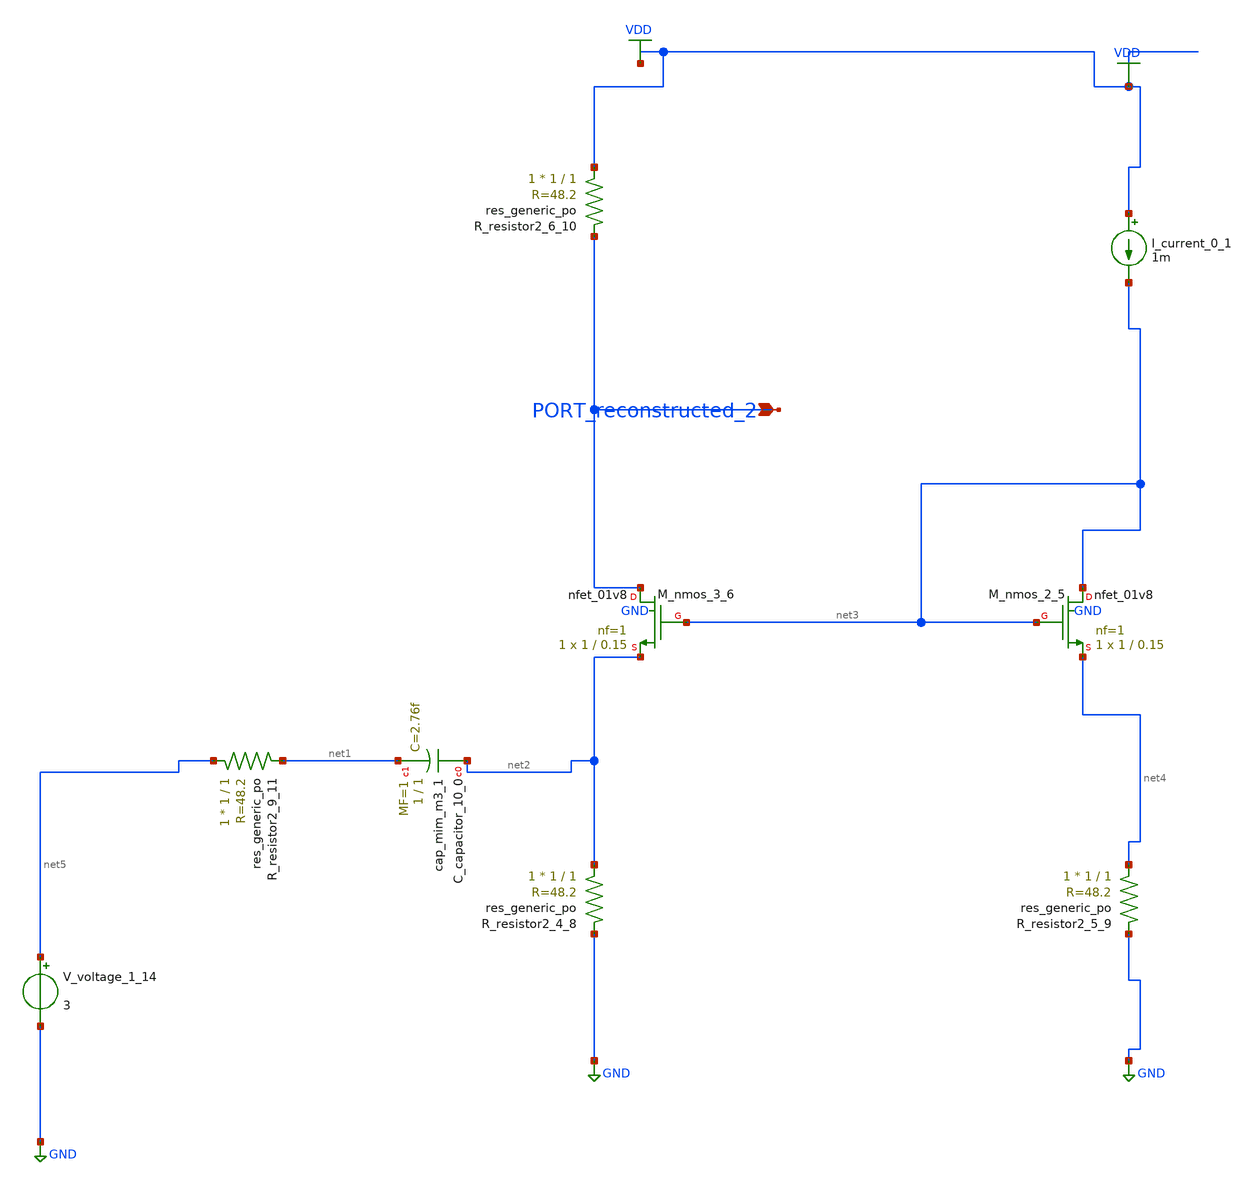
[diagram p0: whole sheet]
** sch_path: schematics/AMSNet/312.sch
**.subckt 312 PORT_reconstructed_2
*.ipin PORT_reconstructed_2
XC_capacitor_10_0 net2 net1 sky130_fd_pr__cap_mim_m3_1 W=1 L=1 MF=1 m=1
I_current_0_1 VDD net3 1m
XM_nmos_2_5 net3 net3 net4 GND sky130_fd_pr__nfet_01v8 L=0.15 W=1 nf=1 ad='int((1 + 1)/2) * 1 / 1 * 0.29'
+ as='int((1 + 2)/2) * 1 / 1 * 0.29' pd='2*int((1 + 1)/2) * (1 / 1 + 0.29)' ps='2*int((1 + 2)/2) * (1 / 1 + 0.29)'
+ nrd='0.29 / 1 ' nrs='0.29 / 1 ' sa=0 sb=0 sd=0 mult=1 m=1
XM_nmos_3_6 PORT_reconstructed_2 net3 net2 GND sky130_fd_pr__nfet_01v8 L=0.15 W=1 nf=1 ad='int((1 + 1)/2) * 1 / 1 * 0.29'
+ as='int((1 + 2)/2) * 1 / 1 * 0.29' pd='2*int((1 + 1)/2) * (1 / 1 + 0.29)' ps='2*int((1 + 2)/2) * (1 / 1 + 0.29)'
+ nrd='0.29 / 1 ' nrs='0.29 / 1 ' sa=0 sb=0 sd=0 mult=1 m=1
XR_resistor2_4_8 net2 GND sky130_fd_pr__res_generic_po W=1 L=1 m=1
XR_resistor2_5_9 net4 GND sky130_fd_pr__res_generic_po W=1 L=1 m=1
XR_resistor2_6_10 VDD PORT_reconstructed_2 sky130_fd_pr__res_generic_po W=1 L=1 m=1
XR_resistor2_9_11 net5 net1 sky130_fd_pr__res_generic_po W=1 L=1 m=1
V_voltage_1_14 net5 GND 3
**.ends
.GLOBAL GND
.GLOBAL VDD
.end
